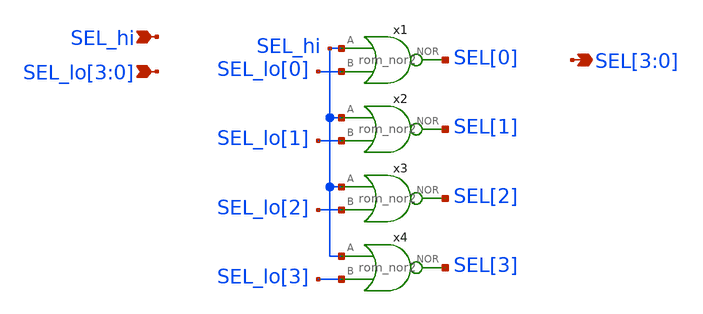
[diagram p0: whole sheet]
** sch_path: blocks/rom/rom_dec_nor.sch
**.subckt rom_dec_nor SEL[3],SEL[2],SEL[1],SEL[0] SEL_hi SEL_lo[3],SEL_lo[2],SEL_lo[1],SEL_lo[0]
*.opin SEL[3],SEL[2],SEL[1],SEL[0]
*.ipin SEL_hi
*.ipin SEL_lo[3],SEL_lo[2],SEL_lo[1],SEL_lo[0]
x2 SEL_hi SEL_lo[1] SEL[1] rom_nor2
x1 SEL_hi SEL_lo[0] SEL[0] rom_nor2
x4 SEL_hi SEL_lo[3] SEL[3] rom_nor2
x3 SEL_hi SEL_lo[2] SEL[2] rom_nor2
**.ends

* expanding   symbol:  rom_nor2.sym # of pins=3
** sym_path: blocks/rom/rom_nor2.sym
** sch_path: blocks/rom/rom_nor2.sch
.subckt rom_nor2 A B NOR
*.ipin A
*.opin NOR
*.ipin B
XM4 net1 A VCC VCC sky130_fd_pr__pfet_01v8 L=0.15 W=1 nf=1 ad='int((nf+1)/2) * W/nf * 0.29' as='int((nf+2)/2) * W/nf * 0.29'
+ pd='2*int((nf+1)/2) * (W/nf + 0.29)' ps='2*int((nf+2)/2) * (W/nf + 0.29)' nrd='0.29 / W' nrs='0.29 / W'
+ sa=0 sb=0 sd=0 mult=1 m=1
XM5 NOR B net1 net1 sky130_fd_pr__pfet_01v8 L=0.15 W=1 nf=1 ad='int((nf+1)/2) * W/nf * 0.29' as='int((nf+2)/2) * W/nf * 0.29'
+ pd='2*int((nf+1)/2) * (W/nf + 0.29)' ps='2*int((nf+2)/2) * (W/nf + 0.29)' nrd='0.29 / W' nrs='0.29 / W'
+ sa=0 sb=0 sd=0 mult=1 m=1
XM9 NOR B VSS VSS sky130_fd_pr__nfet_01v8 L=0.15 W=0.65 nf=1 ad='int((1 + 1)/2) * 0.65 / 1 * 0.29' as='int((1 + 2)/2) * 0.65 / 1 * 0.29'
+ pd='2*int((1 + 1)/2) * (0.65 / 1 + 0.29)' ps='2*int((1 + 2)/2) * (0.65 / 1 + 0.29)' nrd='0.29 / 0.65 '
+ nrs='0.29 / 0.65 ' sa=0 sb=0 sd=0 mult=1 m=1
XM10 NOR A VSS VSS sky130_fd_pr__nfet_01v8 L=0.15 W=0.65 nf=1 ad='int((1 + 1)/2) * 0.65 / 1 * 0.29' as='int((1 + 2)/2) * 0.65 / 1 * 0.29'
+ pd='2*int((1 + 1)/2) * (0.65 / 1 + 0.29)' ps='2*int((1 + 2)/2) * (0.65 / 1 + 0.29)' nrd='0.29 / 0.65 '
+ nrs='0.29 / 0.65 ' sa=0 sb=0 sd=0 mult=1 m=1
.ends

.GLOBAL VCC
.GLOBAL VSS
.end
